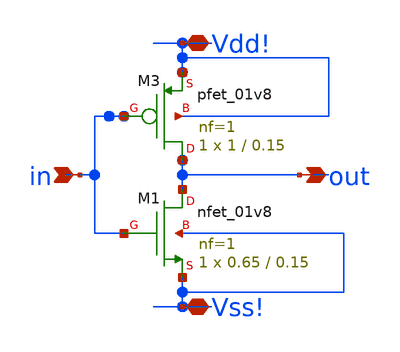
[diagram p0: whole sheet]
** sch_path: inverter_simulation/inv1.sch
**.subckt inv1 Vdd! Vss! in out
*.iopin Vdd!
*.iopin Vss!
*.ipin in
*.opin out
XM1 out in Vss! Vss! sky130_fd_pr__nfet_01v8 L=0.15 W=0.65 nf=1 ad='int((nf+1)/2) * W/nf * 0.29' as='int((nf+2)/2) * W/nf * 0.29'
+ pd='2*int((nf+1)/2) * (W/nf + 0.29)' ps='2*int((nf+2)/2) * (W/nf + 0.29)' nrd='0.29 / W' nrs='0.29 / W'
+ sa=0 sb=0 sd=0 mult=1 m=1
XM3 out in Vdd! Vdd! sky130_fd_pr__pfet_01v8 L=0.15 W=1 nf=1 ad='int((nf+1)/2) * W/nf * 0.29' as='int((nf+2)/2) * W/nf * 0.29'
+ pd='2*int((nf+1)/2) * (W/nf + 0.29)' ps='2*int((nf+2)/2) * (W/nf + 0.29)' nrd='0.29 / W' nrs='0.29 / W'
+ sa=0 sb=0 sd=0 mult=1 m=1
**.ends
.end
